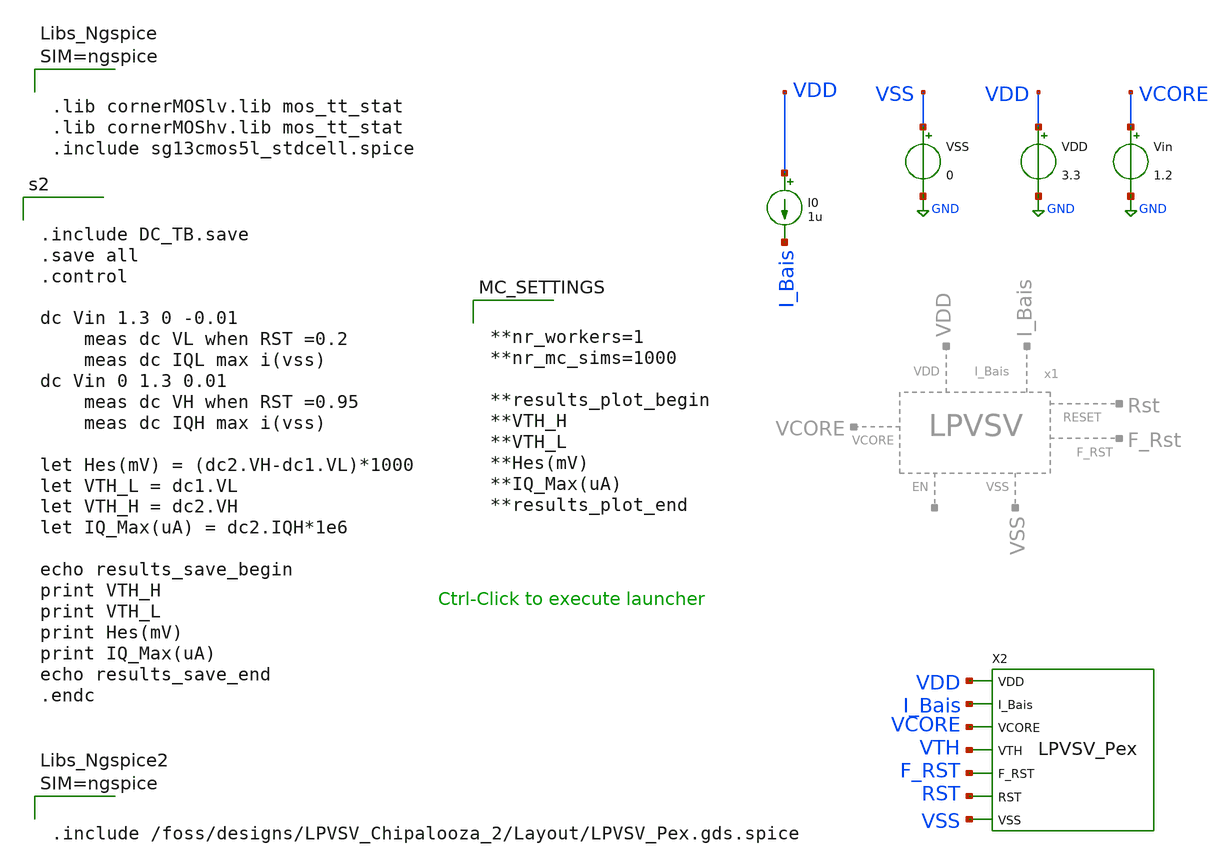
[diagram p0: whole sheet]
** sch_path: Simulation/DC_TB_MC.sch
**.subckt DC_TB_MC
VDD VDD GND 3.3
VSS VSS GND 0
Vin VCORE GND 1.2
I0 VDD I_Bais 1u
X2 F_RST VDD VCORE VSS I_Bais VTH RST LPVSV_Pex
**** begin user architecture code


.include DC_TB.save
.save all
.control

dc Vin 1.3 0 -0.01
	meas dc VL when RST =0.2
	meas dc IQL max i(vss)
dc Vin 0 1.3 0.01
	meas dc VH when RST =0.95
	meas dc IQH max i(vss)

let Hes(mV) = (dc2.VH-dc1.VL)*1000
let VTH_L = dc1.VL
let VTH_H = dc2.VH
let IQ_Max(uA) = dc2.IQH*1e6

echo results_save_begin
print VTH_H
print VTH_L
print Hes(mV)
print IQ_Max(uA)
echo results_save_end
.endc




.options rshunt = 1e15
.options gmin=1e-9
.options reltol = 0.01 abstol = 1p
.option filetype=ascii





.lib cornerMOSlv.lib mos_tt_stat
.lib cornerMOShv.lib mos_tt_stat
.include sg13cmos5l_stdcell.spice





**nr_workers=1
**nr_mc_sims=1000

**results_plot_begin
**VTH_H
**VTH_L
**Hes(mV)
**IQ_Max(uA)
**results_plot_end





.include /foss/designs/LPVSV_Chipalooza_2/Layout/LPVSV_Pex.gds.spice



**** end user architecture code
**.ends
.GLOBAL GND
.end
